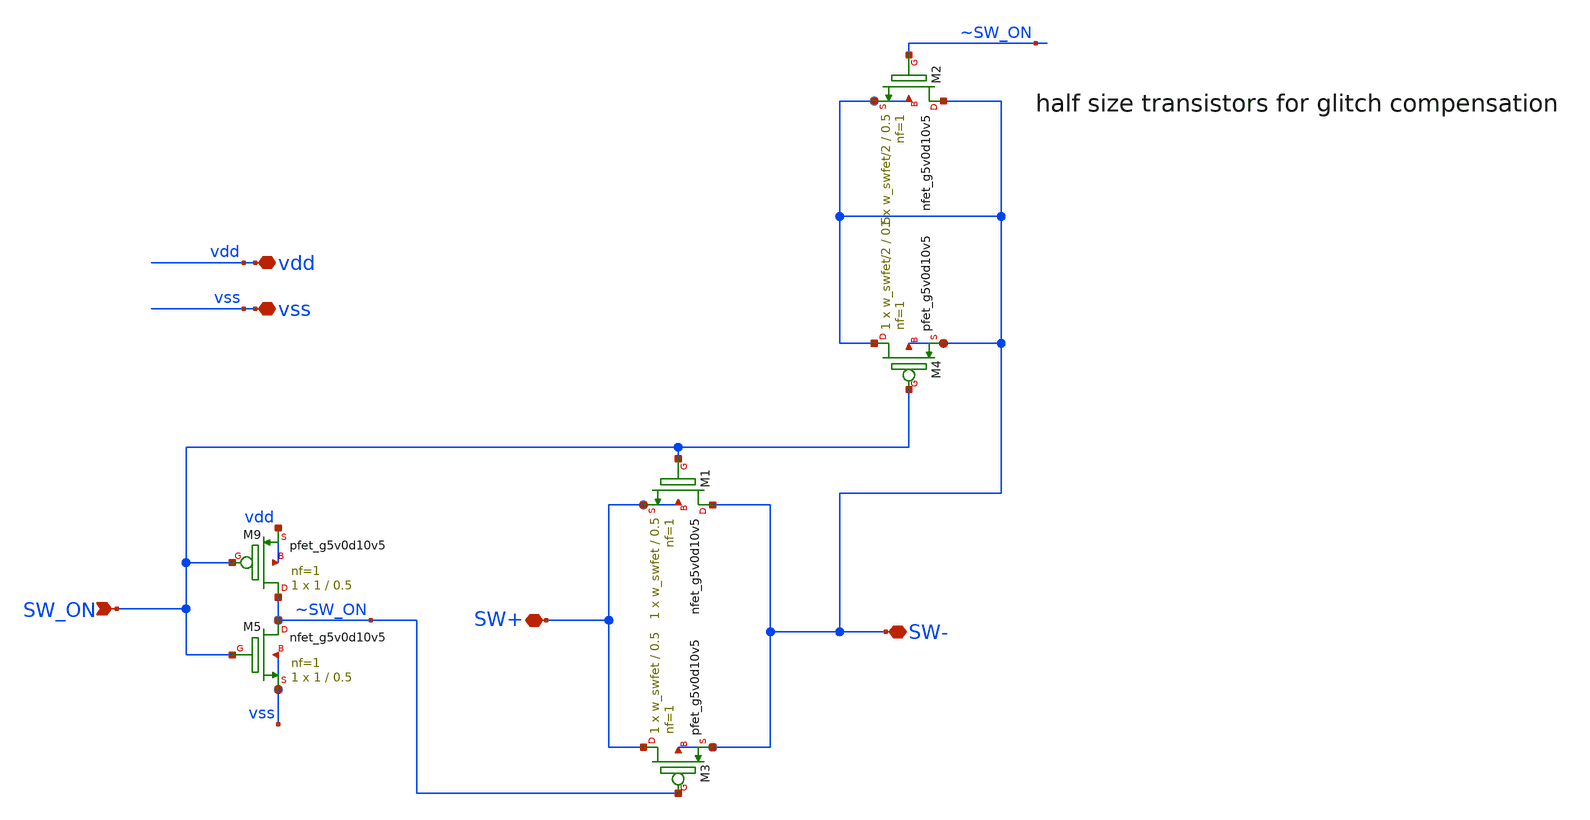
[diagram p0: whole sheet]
** sch_path: xschem/analog_switch.sch
**.subckt analog_switch vdd vss SW_ON SW+ SW-
*.iopin vdd
*.iopin vss
*.ipin SW_ON
*.iopin SW+
*.iopin SW-
XM5 ~SW_ON SW_ON vss vss sky130_fd_pr__nfet_g5v0d10v5 L=0.5 W=1 nf=1 ad='int((1 + 1)/2) * 1 / 1 * 0.29'
+ as='int((1 + 2)/2) * 1 / 1 * 0.29' pd='2*int((1 + 1)/2) * (1 / 1 + 0.29)' ps='2*int((1 + 2)/2) * (1 / 1 + 0.29)'
+ nrd='0.29 / 1 ' nrs='0.29 / 1 ' sa=0 sb=0 sd=0 mult=1 m=1
XM9 ~SW_ON SW_ON vdd vdd sky130_fd_pr__pfet_g5v0d10v5 L=0.5 W=1 nf=1 ad='int((1 + 1)/2) * 1 / 1 * 0.29'
+ as='int((1 + 2)/2) * 1 / 1 * 0.29' pd='2*int((1 + 1)/2) * (1 / 1 + 0.29)' ps='2*int((1 + 2)/2) * (1 / 1 + 0.29)'
+ nrd='0.29 / 1 ' nrs='0.29 / 1 ' sa=0 sb=0 sd=0 mult=1 m=1
XM1 SW- SW_ON SW+ SW+ sky130_fd_pr__nfet_g5v0d10v5 L=0.5 W=w_swfet nf=1 ad='int((1 + 1)/2) * w_swfet / 1 * 0.29'
+ as='int((1 + 2)/2) * w_swfet / 1 * 0.29' pd='2*int((1 + 1)/2) * (w_swfet / 1 + 0.29)' ps='2*int((1 + 2)/2) * (w_swfet / 1 + 0.29)'
+ nrd='0.29 / w_swfet ' nrs='0.29 / w_swfet ' sa=0 sb=0 sd=0 mult=1 m=1
XM3 SW+ ~SW_ON SW- SW- sky130_fd_pr__pfet_g5v0d10v5 L=0.5 W=w_swfet nf=1 ad='int((1 + 1)/2) * w_swfet / 1 * 0.29'
+ as='int((1 + 2)/2) * w_swfet / 1 * 0.29' pd='2*int((1 + 1)/2) * (w_swfet / 1 + 0.29)' ps='2*int((1 + 2)/2) * (w_swfet / 1 + 0.29)'
+ nrd='0.29 / w_swfet ' nrs='0.29 / w_swfet ' sa=0 sb=0 sd=0 mult=1 m=1
XM2 SW- ~SW_ON SW- SW- sky130_fd_pr__nfet_g5v0d10v5 L=0.5 W=w_swfet/2 nf=1 ad='int((1 + 1)/2) * w_swfet/2 / 1 * 0.29'
+ as='int((1 + 2)/2) * w_swfet/2 / 1 * 0.29' pd='2*int((1 + 1)/2) * (w_swfet/2 / 1 + 0.29)' ps='2*int((1 + 2)/2) * (w_swfet/2 / 1 + 0.29)'
+ nrd='0.29 / w_swfet/2 ' nrs='0.29 / w_swfet/2 ' sa=0 sb=0 sd=0 mult=1 m=1
XM4 SW- SW_ON SW- SW- sky130_fd_pr__pfet_g5v0d10v5 L=0.5 W=w_swfet/2 nf=1 ad='int((1 + 1)/2) * w_swfet/2 / 1 * 0.29'
+ as='int((1 + 2)/2) * w_swfet/2 / 1 * 0.29' pd='2*int((1 + 1)/2) * (w_swfet/2 / 1 + 0.29)' ps='2*int((1 + 2)/2) * (w_swfet/2 / 1 + 0.29)'
+ nrd='0.29 / w_swfet/2 ' nrs='0.29 / w_swfet/2 ' sa=0 sb=0 sd=0 mult=1 m=1
**** begin user architecture code
w_swfets=16
**** end user architecture code
**.ends
.end
